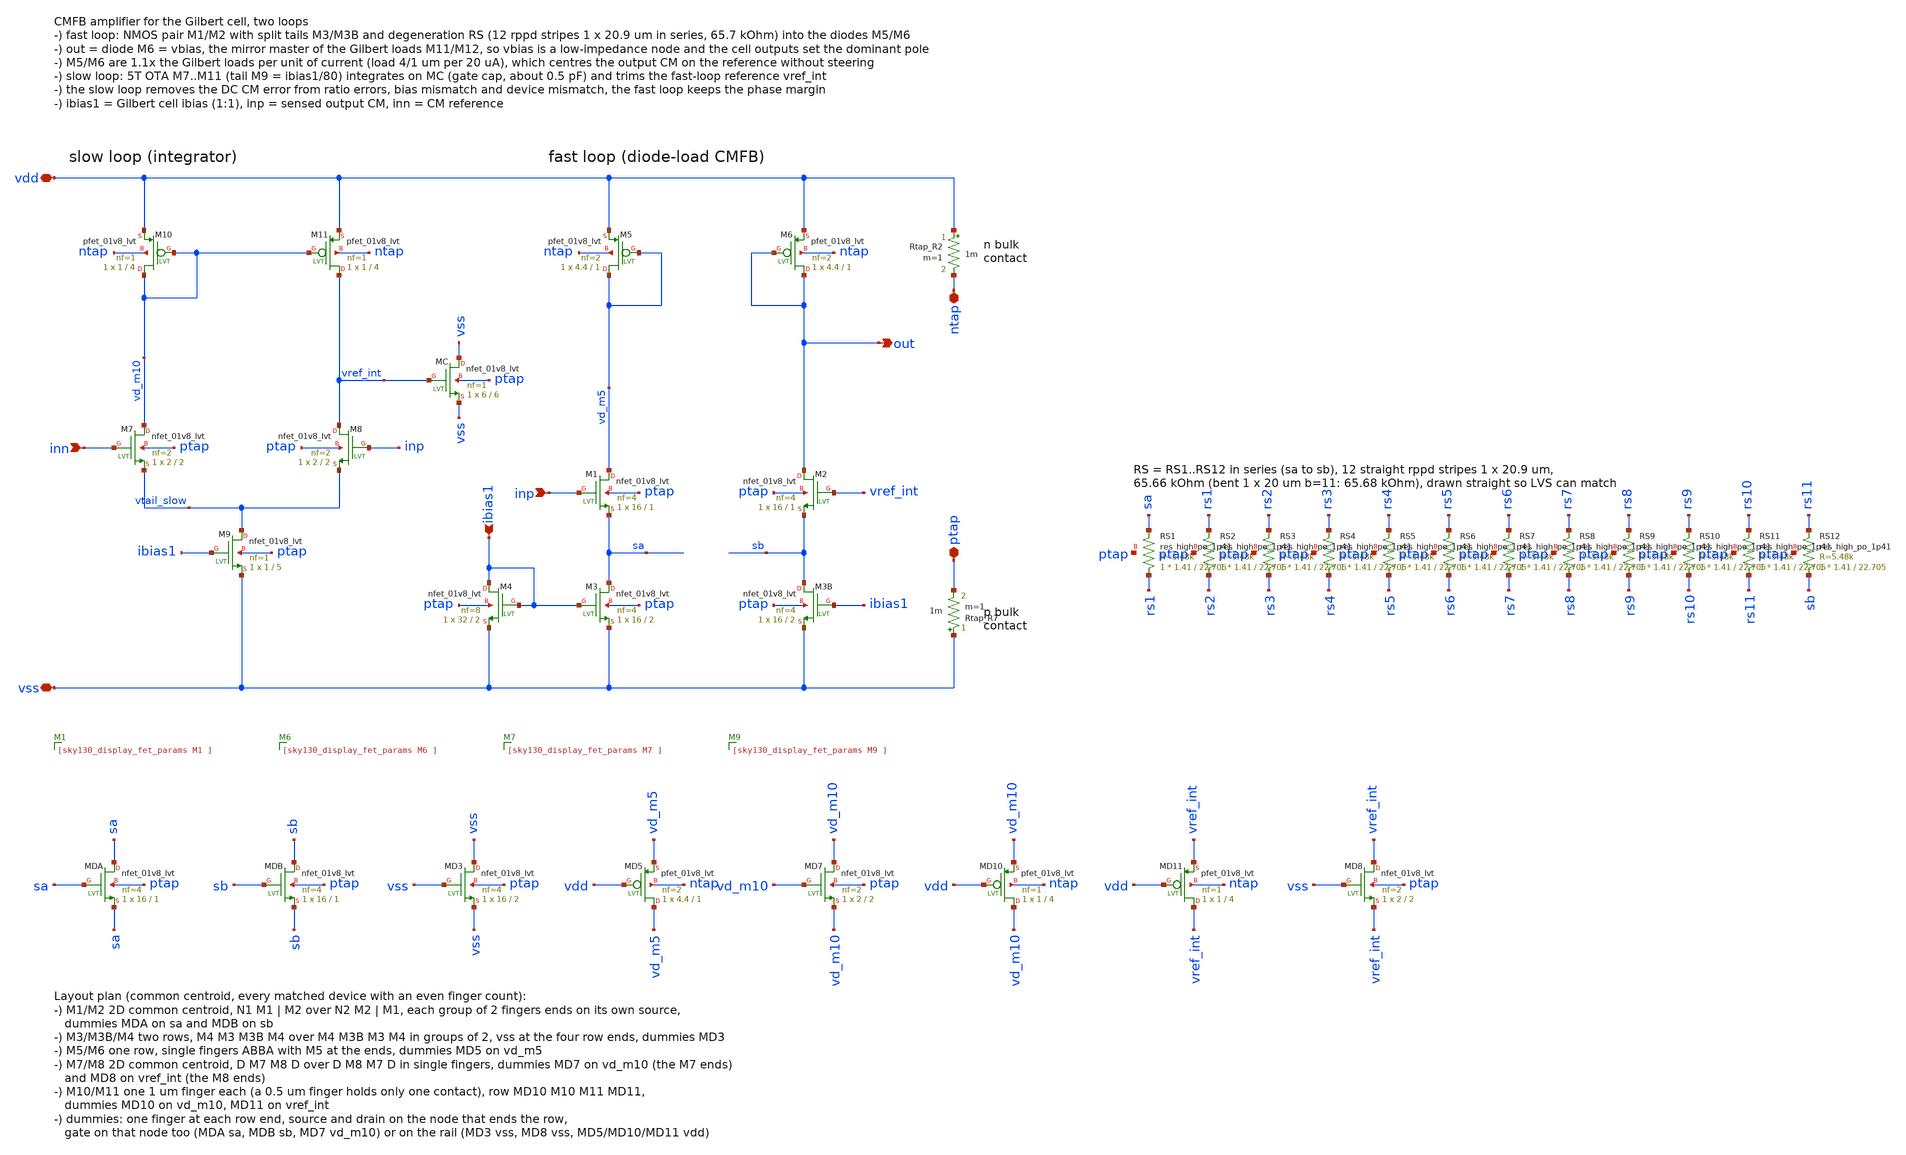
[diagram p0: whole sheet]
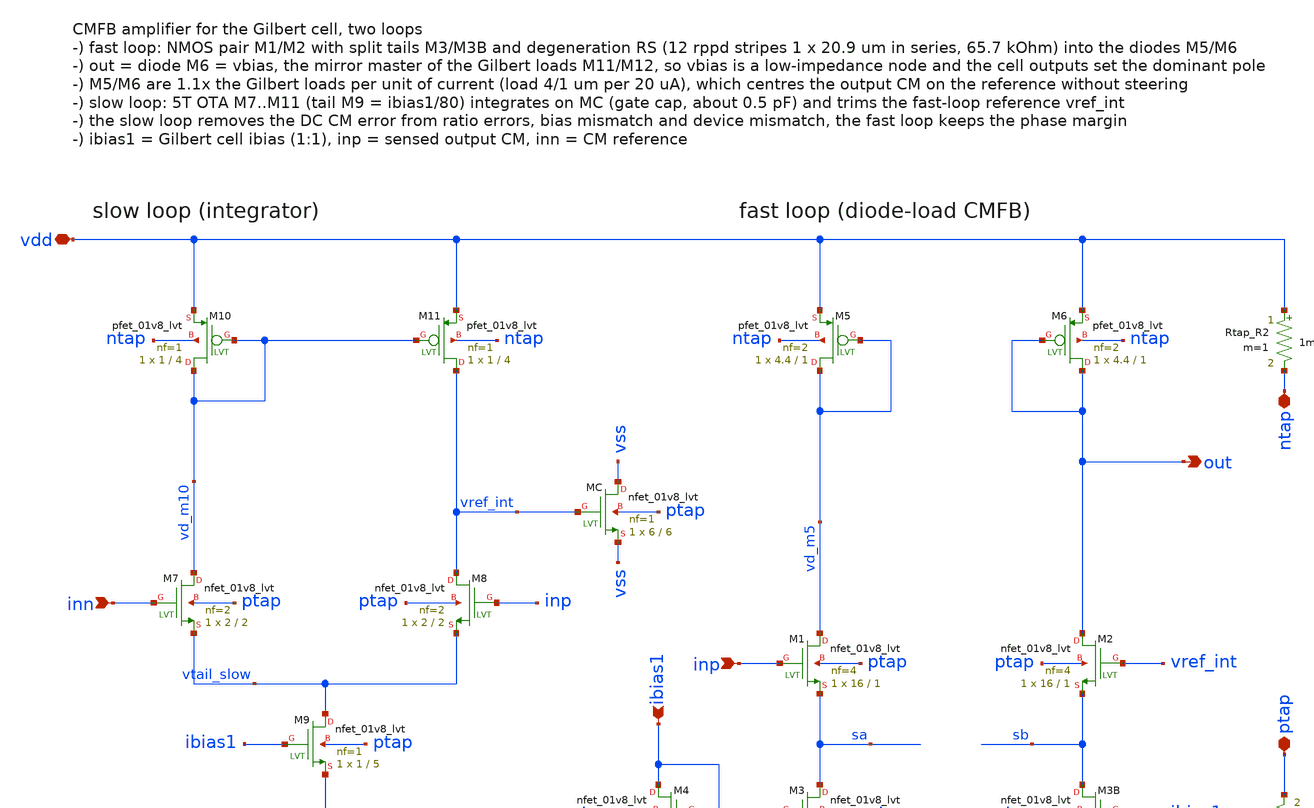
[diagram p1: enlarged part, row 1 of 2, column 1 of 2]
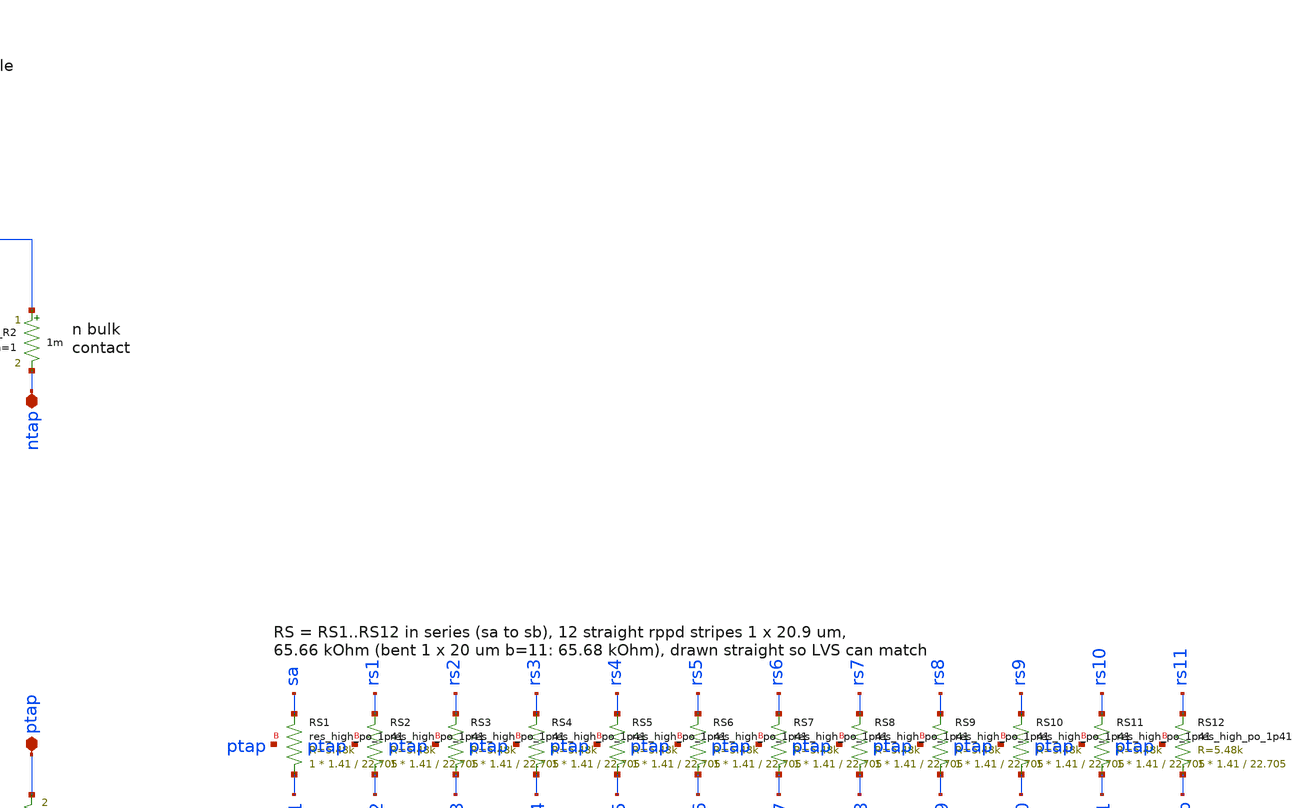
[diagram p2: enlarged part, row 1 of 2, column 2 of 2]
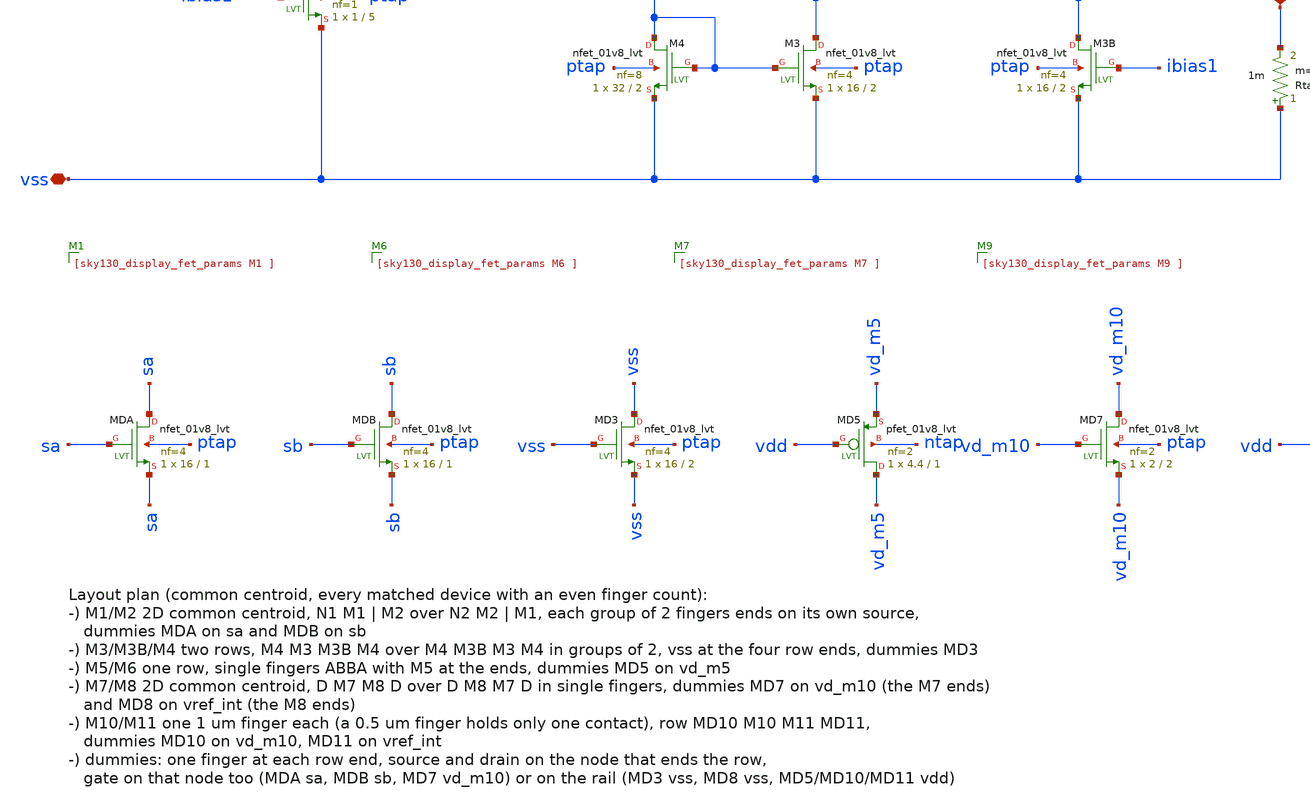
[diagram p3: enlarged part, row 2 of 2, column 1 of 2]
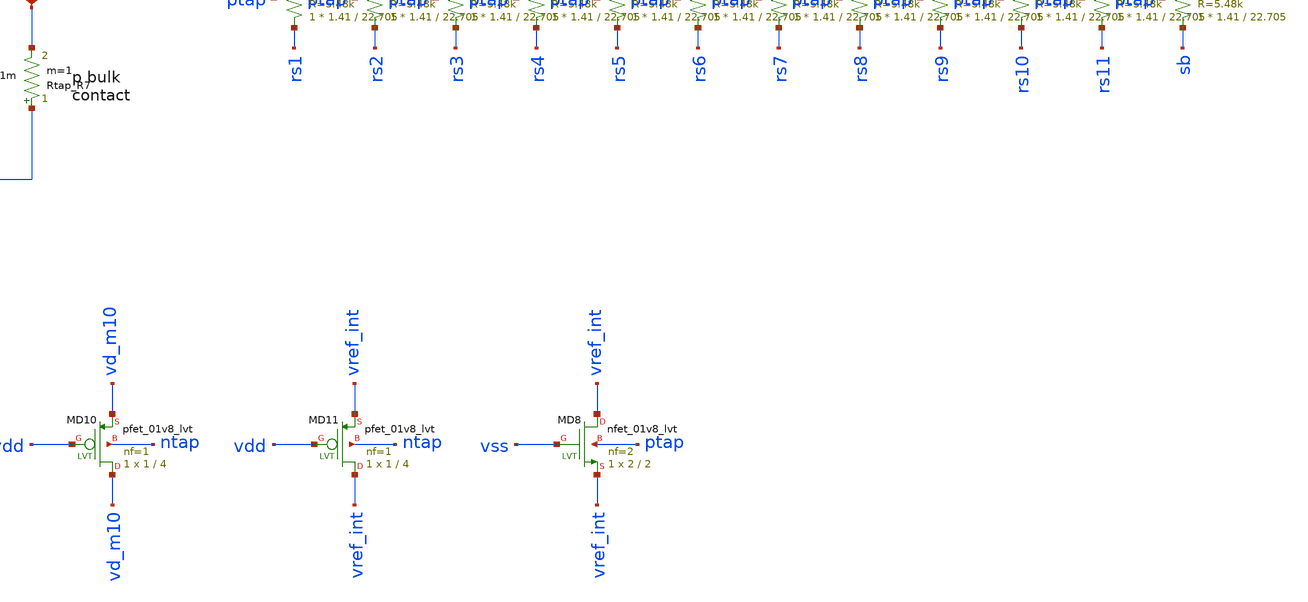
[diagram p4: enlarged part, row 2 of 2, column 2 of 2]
** sch_path: macros/ota/schematic/xschem/ota.sch
**.subckt ota out inp ibias1 inn ntap ptap vdd vss
*.opin out
*.ipin inp
*.ipin ibias1
*.ipin inn
*.iopin ntap
*.iopin ptap
*.iopin vdd
*.iopin vss
XM5 vd_m5 vd_m5 vdd ntap sky130_fd_pr__pfet_01v8_lvt L=1 W=4.4 nf=2 ad='int((2 + 1)/2) * 4.4 / 2 * 0.29'
+ as='int((2 + 2)/2) * 4.4 / 2 * 0.29' pd='2*int((2 + 1)/2) * (4.4 / 2 + 0.29)' ps='2*int((2 + 2)/2) * (4.4 / 2 + 0.29)'
+ nrd='0.29 / 4.4 ' nrs='0.29 / 4.4 ' sa=0 sb=0 sd=0 mult=1 m=1
XM6 out out vdd ntap sky130_fd_pr__pfet_01v8_lvt L=1 W=4.4 nf=2 ad='int((2 + 1)/2) * 4.4 / 2 * 0.29'
+ as='int((2 + 2)/2) * 4.4 / 2 * 0.29' pd='2*int((2 + 1)/2) * (4.4 / 2 + 0.29)' ps='2*int((2 + 2)/2) * (4.4 / 2 + 0.29)'
+ nrd='0.29 / 4.4 ' nrs='0.29 / 4.4 ' sa=0 sb=0 sd=0 mult=1 m=1
XM1 vd_m5 inp sa ptap sky130_fd_pr__nfet_01v8_lvt L=1 W=16 nf=4 ad='int((4 + 1)/2) * 16 / 4 * 0.29' as='int((4 + 2)/2) * 16 / 4 * 0.29'
+ pd='2*int((4 + 1)/2) * (16 / 4 + 0.29)' ps='2*int((4 + 2)/2) * (16 / 4 + 0.29)' nrd='0.29 / 16 ' nrs='0.29 / 16 '
+ sa=0 sb=0 sd=0 mult=1 m=1
XM2 out vref_int sb ptap sky130_fd_pr__nfet_01v8_lvt L=1 W=16 nf=4 ad='int((4 + 1)/2) * 16 / 4 * 0.29'
+ as='int((4 + 2)/2) * 16 / 4 * 0.29' pd='2*int((4 + 1)/2) * (16 / 4 + 0.29)' ps='2*int((4 + 2)/2) * (16 / 4 + 0.29)'
+ nrd='0.29 / 16 ' nrs='0.29 / 16 ' sa=0 sb=0 sd=0 mult=1 m=1
XRS1 rs1 sa ptap sky130_fd_pr__res_high_po_1p41 L=22.705 mult=1 m=1
XRS2 rs2 rs1 ptap sky130_fd_pr__res_high_po_1p41 L=22.705 mult=1 m=1
XRS3 rs3 rs2 ptap sky130_fd_pr__res_high_po_1p41 L=22.705 mult=1 m=1
XRS4 rs4 rs3 ptap sky130_fd_pr__res_high_po_1p41 L=22.705 mult=1 m=1
XRS5 rs5 rs4 ptap sky130_fd_pr__res_high_po_1p41 L=22.705 mult=1 m=1
XRS6 rs6 rs5 ptap sky130_fd_pr__res_high_po_1p41 L=22.705 mult=1 m=1
XRS7 rs7 rs6 ptap sky130_fd_pr__res_high_po_1p41 L=22.705 mult=1 m=1
XRS8 rs8 rs7 ptap sky130_fd_pr__res_high_po_1p41 L=22.705 mult=1 m=1
XRS9 rs9 rs8 ptap sky130_fd_pr__res_high_po_1p41 L=22.705 mult=1 m=1
XRS10 rs10 rs9 ptap sky130_fd_pr__res_high_po_1p41 L=22.705 mult=1 m=1
XRS11 rs11 rs10 ptap sky130_fd_pr__res_high_po_1p41 L=22.705 mult=1 m=1
XRS12 sb rs11 ptap sky130_fd_pr__res_high_po_1p41 L=22.705 mult=1 m=1
XM3 sa ibias1 vss ptap sky130_fd_pr__nfet_01v8_lvt L=2 W=16 nf=4 ad='int((4 + 1)/2) * 16 / 4 * 0.29'
+ as='int((4 + 2)/2) * 16 / 4 * 0.29' pd='2*int((4 + 1)/2) * (16 / 4 + 0.29)' ps='2*int((4 + 2)/2) * (16 / 4 + 0.29)'
+ nrd='0.29 / 16 ' nrs='0.29 / 16 ' sa=0 sb=0 sd=0 mult=1 m=1
XM3B sb ibias1 vss ptap sky130_fd_pr__nfet_01v8_lvt L=2 W=16 nf=4 ad='int((4 + 1)/2) * 16 / 4 * 0.29'
+ as='int((4 + 2)/2) * 16 / 4 * 0.29' pd='2*int((4 + 1)/2) * (16 / 4 + 0.29)' ps='2*int((4 + 2)/2) * (16 / 4 + 0.29)'
+ nrd='0.29 / 16 ' nrs='0.29 / 16 ' sa=0 sb=0 sd=0 mult=1 m=1
XM4 ibias1 ibias1 vss ptap sky130_fd_pr__nfet_01v8_lvt L=2 W=32 nf=8 ad='int((8 + 1)/2) * 32 / 8 * 0.29'
+ as='int((8 + 2)/2) * 32 / 8 * 0.29' pd='2*int((8 + 1)/2) * (32 / 8 + 0.29)' ps='2*int((8 + 2)/2) * (32 / 8 + 0.29)'
+ nrd='0.29 / 32 ' nrs='0.29 / 32 ' sa=0 sb=0 sd=0 mult=1 m=1
XM10 vd_m10 vd_m10 vdd ntap sky130_fd_pr__pfet_01v8_lvt L=4 W=1 nf=1 ad='int((1 + 1)/2) * 1 / 1 * 0.29'
+ as='int((1 + 2)/2) * 1 / 1 * 0.29' pd='2*int((1 + 1)/2) * (1 / 1 + 0.29)' ps='2*int((1 + 2)/2) * (1 / 1 + 0.29)'
+ nrd='0.29 / 1 ' nrs='0.29 / 1 ' sa=0 sb=0 sd=0 mult=1 m=1
XM11 vref_int vd_m10 vdd ntap sky130_fd_pr__pfet_01v8_lvt L=4 W=1 nf=1 ad='int((1 + 1)/2) * 1 / 1 * 0.29'
+ as='int((1 + 2)/2) * 1 / 1 * 0.29' pd='2*int((1 + 1)/2) * (1 / 1 + 0.29)' ps='2*int((1 + 2)/2) * (1 / 1 + 0.29)'
+ nrd='0.29 / 1 ' nrs='0.29 / 1 ' sa=0 sb=0 sd=0 mult=1 m=1
XM7 vd_m10 inn vtail_slow ptap sky130_fd_pr__nfet_01v8_lvt L=2 W=2 nf=2 ad='int((2 + 1)/2) * 2 / 2 * 0.29'
+ as='int((2 + 2)/2) * 2 / 2 * 0.29' pd='2*int((2 + 1)/2) * (2 / 2 + 0.29)' ps='2*int((2 + 2)/2) * (2 / 2 + 0.29)'
+ nrd='0.29 / 2 ' nrs='0.29 / 2 ' sa=0 sb=0 sd=0 mult=1 m=1
XM8 vref_int inp vtail_slow ptap sky130_fd_pr__nfet_01v8_lvt L=2 W=2 nf=2 ad='int((2 + 1)/2) * 2 / 2 * 0.29'
+ as='int((2 + 2)/2) * 2 / 2 * 0.29' pd='2*int((2 + 1)/2) * (2 / 2 + 0.29)' ps='2*int((2 + 2)/2) * (2 / 2 + 0.29)'
+ nrd='0.29 / 2 ' nrs='0.29 / 2 ' sa=0 sb=0 sd=0 mult=1 m=1
XM9 vtail_slow ibias1 vss ptap sky130_fd_pr__nfet_01v8_lvt L=5 W=1 nf=1 ad='int((1 + 1)/2) * 1 / 1 * 0.29'
+ as='int((1 + 2)/2) * 1 / 1 * 0.29' pd='2*int((1 + 1)/2) * (1 / 1 + 0.29)' ps='2*int((1 + 2)/2) * (1 / 1 + 0.29)'
+ nrd='0.29 / 1 ' nrs='0.29 / 1 ' sa=0 sb=0 sd=0 mult=1 m=1
XMC vss vref_int vss ptap sky130_fd_pr__nfet_01v8_lvt L=6 W=6 nf=1 ad='int((1 + 1)/2) * 6 / 1 * 0.29'
+ as='int((1 + 2)/2) * 6 / 1 * 0.29' pd='2*int((1 + 1)/2) * (6 / 1 + 0.29)' ps='2*int((1 + 2)/2) * (6 / 1 + 0.29)'
+ nrd='0.29 / 6 ' nrs='0.29 / 6 ' sa=0 sb=0 sd=0 mult=1 m=1
Rtap_R2 vdd ntap 1m m=1
Rtap_R7 vss ptap 1m m=1
XMDA sa sa sa ptap sky130_fd_pr__nfet_01v8_lvt L=1 W=16 nf=4 ad='int((4 + 1)/2) * 16 / 4 * 0.29' as='int((4 + 2)/2) * 16 / 4 * 0.29'
+ pd='2*int((4 + 1)/2) * (16 / 4 + 0.29)' ps='2*int((4 + 2)/2) * (16 / 4 + 0.29)' nrd='0.29 / 16 ' nrs='0.29 / 16 '
+ sa=0 sb=0 sd=0 mult=1 m=1
XMDB sb sb sb ptap sky130_fd_pr__nfet_01v8_lvt L=1 W=16 nf=4 ad='int((4 + 1)/2) * 16 / 4 * 0.29' as='int((4 + 2)/2) * 16 / 4 * 0.29'
+ pd='2*int((4 + 1)/2) * (16 / 4 + 0.29)' ps='2*int((4 + 2)/2) * (16 / 4 + 0.29)' nrd='0.29 / 16 ' nrs='0.29 / 16 '
+ sa=0 sb=0 sd=0 mult=1 m=1
XMD3 vss vss vss ptap sky130_fd_pr__nfet_01v8_lvt L=2 W=16 nf=4 ad='int((4 + 1)/2) * 16 / 4 * 0.29' as='int((4 + 2)/2) * 16 / 4 * 0.29'
+ pd='2*int((4 + 1)/2) * (16 / 4 + 0.29)' ps='2*int((4 + 2)/2) * (16 / 4 + 0.29)' nrd='0.29 / 16 ' nrs='0.29 / 16 '
+ sa=0 sb=0 sd=0 mult=1 m=1
XMD5 vd_m5 vdd vd_m5 ntap sky130_fd_pr__pfet_01v8_lvt L=1 W=4.4 nf=2 ad='int((2 + 1)/2) * 4.4 / 2 * 0.29'
+ as='int((2 + 2)/2) * 4.4 / 2 * 0.29' pd='2*int((2 + 1)/2) * (4.4 / 2 + 0.29)' ps='2*int((2 + 2)/2) * (4.4 / 2 + 0.29)'
+ nrd='0.29 / 4.4 ' nrs='0.29 / 4.4 ' sa=0 sb=0 sd=0 mult=1 m=1
XMD7 vd_m10 vd_m10 vd_m10 ptap sky130_fd_pr__nfet_01v8_lvt L=2 W=2 nf=2 ad='int((2 + 1)/2) * 2 / 2 * 0.29'
+ as='int((2 + 2)/2) * 2 / 2 * 0.29' pd='2*int((2 + 1)/2) * (2 / 2 + 0.29)' ps='2*int((2 + 2)/2) * (2 / 2 + 0.29)'
+ nrd='0.29 / 2 ' nrs='0.29 / 2 ' sa=0 sb=0 sd=0 mult=1 m=1
XMD10 vd_m10 vdd vd_m10 ntap sky130_fd_pr__pfet_01v8_lvt L=4 W=1 nf=1 ad='int((1 + 1)/2) * 1 / 1 * 0.29'
+ as='int((1 + 2)/2) * 1 / 1 * 0.29' pd='2*int((1 + 1)/2) * (1 / 1 + 0.29)' ps='2*int((1 + 2)/2) * (1 / 1 + 0.29)'
+ nrd='0.29 / 1 ' nrs='0.29 / 1 ' sa=0 sb=0 sd=0 mult=1 m=1
XMD11 vref_int vdd vref_int ntap sky130_fd_pr__pfet_01v8_lvt L=4 W=1 nf=1 ad='int((1 + 1)/2) * 1 / 1 * 0.29'
+ as='int((1 + 2)/2) * 1 / 1 * 0.29' pd='2*int((1 + 1)/2) * (1 / 1 + 0.29)' ps='2*int((1 + 2)/2) * (1 / 1 + 0.29)'
+ nrd='0.29 / 1 ' nrs='0.29 / 1 ' sa=0 sb=0 sd=0 mult=1 m=1
XMD8 vref_int vss vref_int ptap sky130_fd_pr__nfet_01v8_lvt L=2 W=2 nf=2 ad='int((2 + 1)/2) * 2 / 2 * 0.29'
+ as='int((2 + 2)/2) * 2 / 2 * 0.29' pd='2*int((2 + 1)/2) * (2 / 2 + 0.29)' ps='2*int((2 + 2)/2) * (2 / 2 + 0.29)'
+ nrd='0.29 / 2 ' nrs='0.29 / 2 ' sa=0 sb=0 sd=0 mult=1 m=1
**.ends
.end
